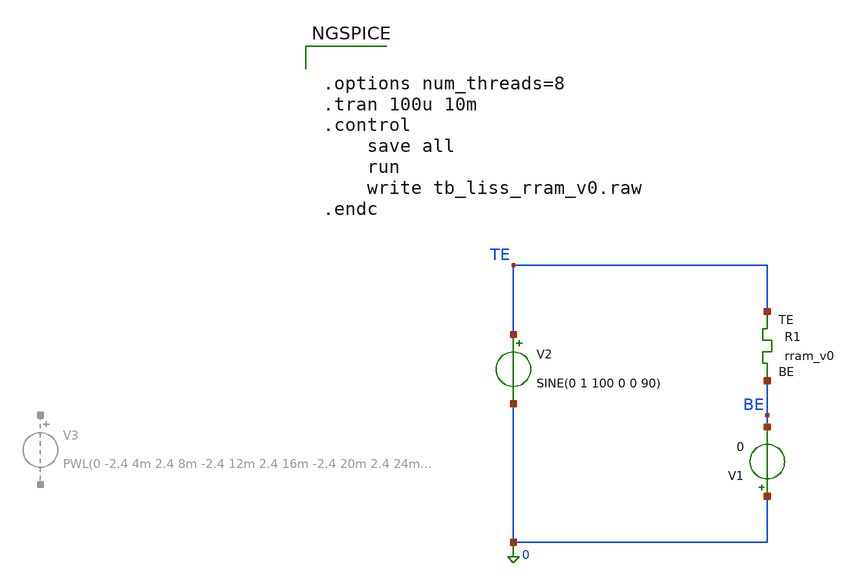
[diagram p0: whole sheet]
** sch_path: memristor_models/wellposed/tb_liss_rram_v0.sch
**.subckt tb_liss_rram_v0
XR1 TE BE rram_v0
V2 TE 0 SINE(0 1 100 0 0 90)
V1 0 BE 0
**** begin user architecture code


.options num_threads=8
.tran 100u 10m
.control
	save all
	run
	write tb_liss_rram_v0.raw
.endc




** opencircuitdesign pdks install
.inc $::SKYWATER_MODELS/rram_v0.spice

**** end user architecture code
**.ends
.end
